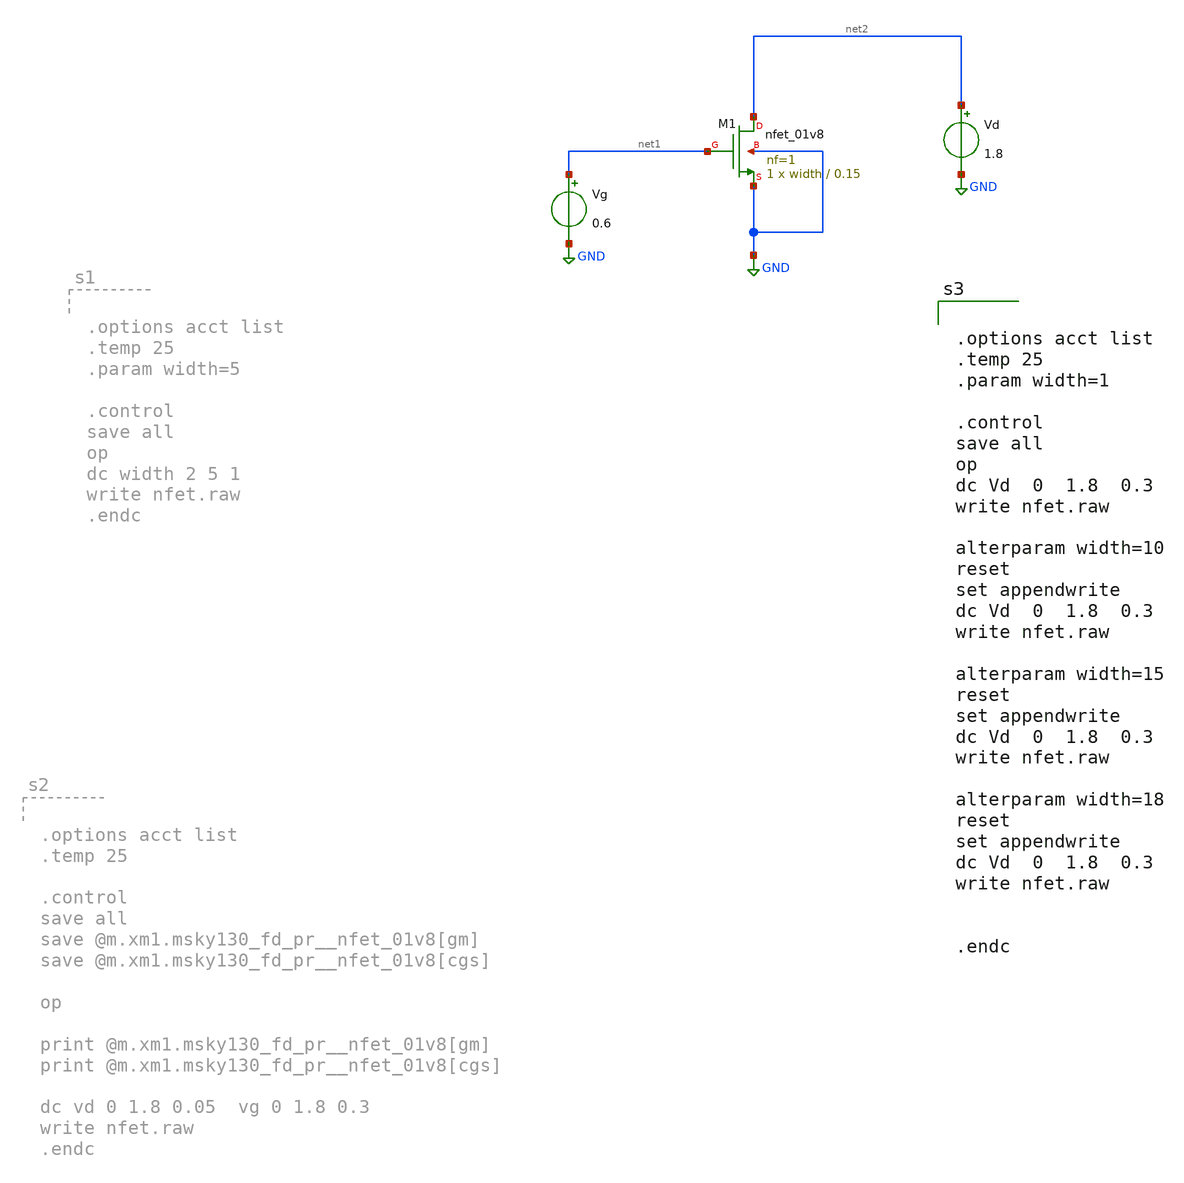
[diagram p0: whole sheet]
** sch_path: xschem/nfet.sch
**.subckt nfet
XM1 net2 net1 GND GND sky130_fd_pr__nfet_01v8 L=0.15 W=width nf=1 ad='int((nf+1)/2) * W/nf * 0.29' as='int((nf+2)/2) * W/nf * 0.29'
+ pd='2*int((nf+1)/2) * (W/nf + 0.29)' ps='2*int((nf+2)/2) * (W/nf + 0.29)' nrd='0.29 / W' nrs='0.29 / W'
+ sa=0 sb=0 sd=0 mult=1 m=1
Vg net1 GND 0.6
Vd net2 GND 1.8
**** begin user architecture code

** opencircuitdesign pdks install
.lib $::SKYWATER_MODELS/sky130.lib.spice tt




.options acct list
.temp 25
.param width=1

.control
save all
op
dc Vd  0  1.8  0.3
write nfet.raw

alterparam width=10
reset
set appendwrite
dc Vd  0  1.8  0.3
write nfet.raw

alterparam width=15
reset
set appendwrite
dc Vd  0  1.8  0.3
write nfet.raw

alterparam width=18
reset
set appendwrite
dc Vd  0  1.8  0.3
write nfet.raw


.endc


**** end user architecture code
**.ends
.GLOBAL GND
.end
